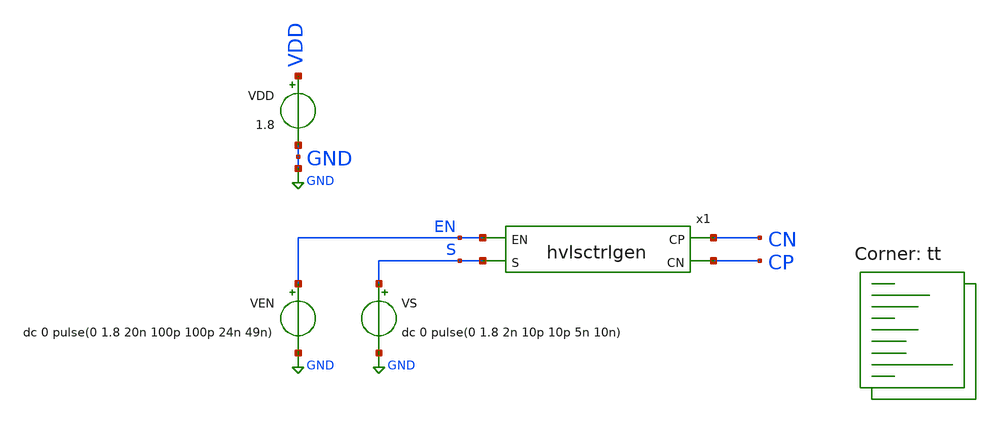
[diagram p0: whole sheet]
** sch_path: test-hvlsctrlgen.sch

.include $::SKYWATER_STDCELLS/sky130_fd_sc_hd.spice

**.subckt test-hvlsctrlgen
x1 EN CN S CP GND GND VDD VDD hvlsctrlgen
VS S GND dc 0 pulse(0 1.8 2n 10p 10p 5n 10n)
VEN EN GND dc 0 pulse(0 1.8 20n 100p 100p 24n 49n)
VDD VDD GND 1.8
**** begin user architecture code
.lib $::SKYWATER_MODELS/sky130.lib.spice tt



.param VDD=1.8
.option savecurrents
.control
  save all
  op
  remzerovec
  write test-hvlsctrlgen.raw
  set appendwrite
  tran 10p 100n
  remzerovec
  write test-hvlsctrlgen.raw
.endc



**** end user architecture code
**.ends

* expanding   symbol:  hvlsctrlgen.sym # of pins=4
** sym_path: hvlsctrlgen.sym
** sch_path: hvlsctrlgen.sch
.subckt hvlsctrlgen EN CP S CN VGND VNB VPB VPWR
*.ipin S
*.ipin EN
*.opin CP
*.opin CN
x1 SDI EN S VGND VNB VPB VPWR CP sky130_fd_sc_hd__and3b_1
x2 S EN SDI VGND VNB VPB VPWR CN sky130_fd_sc_hd__and3b_1
x3 net1 VGND VNB VPB VPWR SDI sky130_fd_sc_hd__inv_1
x4 S VGND VNB VPB VPWR net1 sky130_fd_sc_hd__dlygate4sd1_1
.ends

.GLOBAL GND
.end
